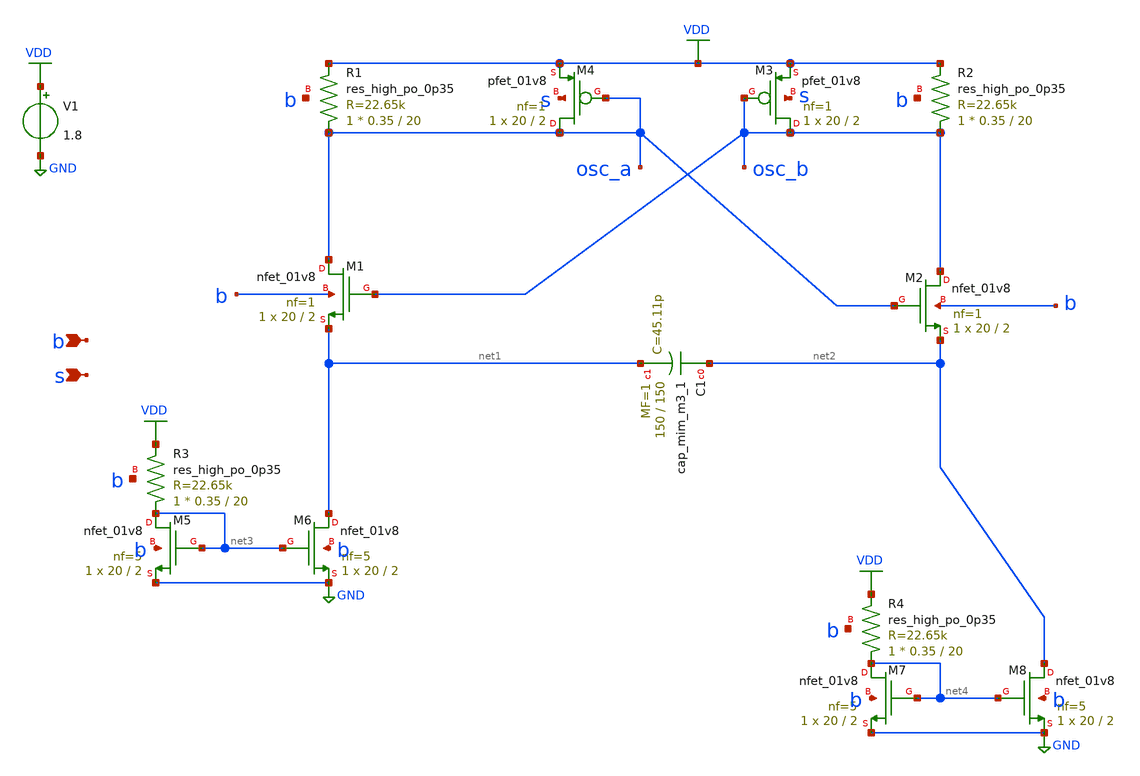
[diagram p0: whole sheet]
** sch_path: xschem/osc.sch
**.subckt osc b s
*.ipin b
*.ipin s
XM1 osc_a osc_b net1 b sky130_fd_pr__nfet_01v8 L=2 W=20 nf=1 ad='int((nf+1)/2) * W/nf * 0.29' as='int((nf+2)/2) * W/nf * 0.29'
+ pd='2*int((nf+1)/2) * (W/nf + 0.29)' ps='2*int((nf+2)/2) * (W/nf + 0.29)' nrd='0.29 / W' nrs='0.29 / W'
+ sa=0 sb=0 sd=0 mult=1 m=1
XM2 osc_b osc_a net2 b sky130_fd_pr__nfet_01v8 L=2 W=20 nf=1 ad='int((nf+1)/2) * W/nf * 0.29' as='int((nf+2)/2) * W/nf * 0.29'
+ pd='2*int((nf+1)/2) * (W/nf + 0.29)' ps='2*int((nf+2)/2) * (W/nf + 0.29)' nrd='0.29 / W' nrs='0.29 / W'
+ sa=0 sb=0 sd=0 mult=1 m=1
XM3 osc_b osc_b VDD s sky130_fd_pr__pfet_01v8 L=2 W=20 nf=1 ad='int((nf+1)/2) * W/nf * 0.29' as='int((nf+2)/2) * W/nf * 0.29'
+ pd='2*int((nf+1)/2) * (W/nf + 0.29)' ps='2*int((nf+2)/2) * (W/nf + 0.29)' nrd='0.29 / W' nrs='0.29 / W'
+ sa=0 sb=0 sd=0 mult=1 m=1
XM4 osc_a osc_a VDD s sky130_fd_pr__pfet_01v8 L=2 W=20 nf=1 ad='int((nf+1)/2) * W/nf * 0.29' as='int((nf+2)/2) * W/nf * 0.29'
+ pd='2*int((nf+1)/2) * (W/nf + 0.29)' ps='2*int((nf+2)/2) * (W/nf + 0.29)' nrd='0.29 / W' nrs='0.29 / W'
+ sa=0 sb=0 sd=0 mult=1 m=1
XR1 osc_a VDD b sky130_fd_pr__res_high_po_0p35 L=20 mult=1 m=1
XR2 osc_b VDD b sky130_fd_pr__res_high_po_0p35 L=20 mult=1 m=1
XC1 net2 net1 sky130_fd_pr__cap_mim_m3_1 W=150 L=150 MF=1 m=1
V1 VDD GND 1.8
XM5 net3 net3 GND b sky130_fd_pr__nfet_01v8 L=2 W=20 nf=5 ad='int((nf+1)/2) * W/nf * 0.29' as='int((nf+2)/2) * W/nf * 0.29'
+ pd='2*int((nf+1)/2) * (W/nf + 0.29)' ps='2*int((nf+2)/2) * (W/nf + 0.29)' nrd='0.29 / W' nrs='0.29 / W'
+ sa=0 sb=0 sd=0 mult=1 m=1
XM6 net1 net3 GND b sky130_fd_pr__nfet_01v8 L=2 W=20 nf=5 ad='int((nf+1)/2) * W/nf * 0.29' as='int((nf+2)/2) * W/nf * 0.29'
+ pd='2*int((nf+1)/2) * (W/nf + 0.29)' ps='2*int((nf+2)/2) * (W/nf + 0.29)' nrd='0.29 / W' nrs='0.29 / W'
+ sa=0 sb=0 sd=0 mult=1 m=1
XR3 net3 VDD b sky130_fd_pr__res_high_po_0p35 L=20 mult=1 m=1
XM7 net4 net4 GND b sky130_fd_pr__nfet_01v8 L=2 W=20 nf=5 ad='int((nf+1)/2) * W/nf * 0.29' as='int((nf+2)/2) * W/nf * 0.29'
+ pd='2*int((nf+1)/2) * (W/nf + 0.29)' ps='2*int((nf+2)/2) * (W/nf + 0.29)' nrd='0.29 / W' nrs='0.29 / W'
+ sa=0 sb=0 sd=0 mult=1 m=1
XM8 net2 net4 GND b sky130_fd_pr__nfet_01v8 L=2 W=20 nf=5 ad='int((nf+1)/2) * W/nf * 0.29' as='int((nf+2)/2) * W/nf * 0.29'
+ pd='2*int((nf+1)/2) * (W/nf + 0.29)' ps='2*int((nf+2)/2) * (W/nf + 0.29)' nrd='0.29 / W' nrs='0.29 / W'
+ sa=0 sb=0 sd=0 mult=1 m=1
XR4 net4 VDD b sky130_fd_pr__res_high_po_0p35 L=20 mult=1 m=1
**** begin user architecture code

** opencircuitdesign pdks install
.lib $::SKYWATER_MODELS/sky130.lib.spice tt




* .options filetype=ascii
.param mc_mm_switch=0
.param mc_pr_switch=0
*.ic V(osc_a)=1 V(osc_b)=0
vs s 1.8 0
vb b 0 0
.control
options method=gear
*reltol=0.1m trtol=1
tran 1n 5000n uic
write testbench.raw
quit 0
.endc
.end


**** end user architecture code
**.ends
.GLOBAL GND
.GLOBAL VDD
.end
